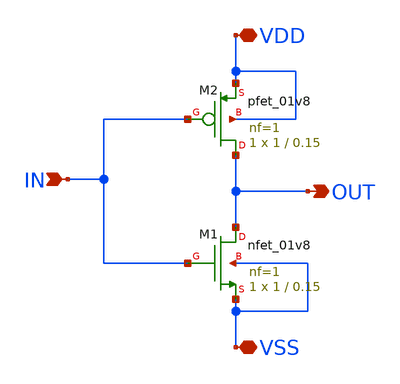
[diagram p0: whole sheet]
** sch_path: xschem/schematic/SCI_DCDL/TG_SCI/inverter.sch
**.subckt inverter IN OUT VDD VSS
*.ipin IN
*.opin OUT
*.iopin VDD
*.iopin VSS
XM1 OUT IN VSS VSS sky130_fd_pr__nfet_01v8 L=0.15 W=1 nf=1 ad='int((1 + 1)/2) * 1 / 1 * 0.29' as='int((1 + 2)/2) * 1 / 1 * 0.29'
+ pd='2*int((1 + 1)/2) * (1 / 1 + 0.29)' ps='2*int((1 + 2)/2) * (1 / 1 + 0.29)' nrd='0.29 / 1 ' nrs='0.29 / 1 '
+ sa=0 sb=0 sd=0 mult=1 m=1
XM2 OUT IN VDD VDD sky130_fd_pr__pfet_01v8 L=0.15 W=1 nf=1 ad='int((1 + 1)/2) * 1 / 1 * 0.29' as='int((1 + 2)/2) * 1 / 1 * 0.29'
+ pd='2*int((1 + 1)/2) * (1 / 1 + 0.29)' ps='2*int((1 + 2)/2) * (1 / 1 + 0.29)' nrd='0.29 / 1 ' nrs='0.29 / 1 '
+ sa=0 sb=0 sd=0 mult=1 m=1
**.ends
.end
